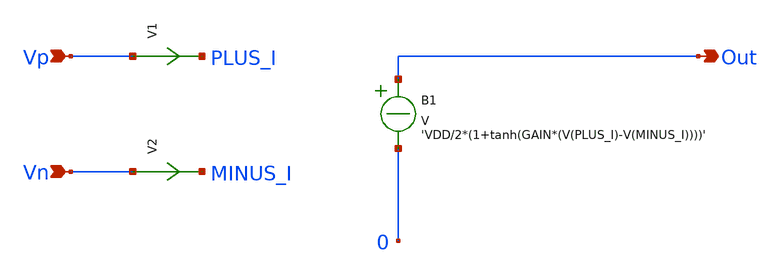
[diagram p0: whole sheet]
** sch_path: Analog_blocks/Analog_Blocks/OTA/Schematic/Ideal_opamp/Ideal_opamp.sch
**.subckt Ideal_opamp Vp Vn Out
*.ipin Vp
*.ipin Vn
*.opin Out
V1 Vp PLUS_I 0
.save i(v1)
V2 Vn MINUS_I 0
.save i(v2)
B1 Out 0 V = 'VDD/2*(1+tanh(GAIN*(V(PLUS_I)-V(MINUS_I))))'
**.ends
.end
